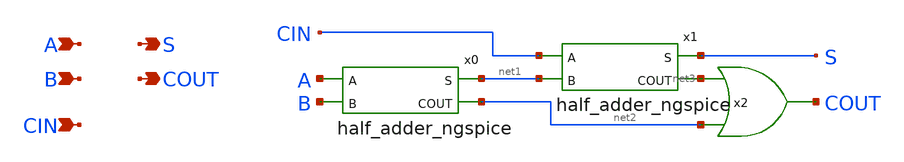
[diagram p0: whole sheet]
** sch_path: xschem_libraries_oa/ngspice/full_adder_ngspice/schematic/full_adder_ngspice.sch
* Copyright (C) 1998-2024 Stefan Frederik Schippers
* This program is free software; you can redistribute it and/or modify
* it under the terms of the GNU General Public License as published by
* the Free Software Foundation; either version 2 of the License, or
* (at your option) any later version.
* This program is distributed in the hope that it will be useful,
* but WITHOUT ANY WARRANTY; without even the implied warranty of
* MERCHANTABILITY or FITNESS FOR A PARTICULAR PURPOSE.  See the
* GNU General Public License for more details.
* You should have received a copy of the GNU General Public License
* along with this program; if not, write to the Free Software
**.subckt full_adder_ngspice A B CIN S COUT
*.ipin A
*.ipin B
*.ipin CIN
*.opin S
*.opin COUT
x0 A net1 net2 B half_adder_ngspice
x1 CIN S net3 net1 half_adder_ngspice
x2 COUT net3 net2 or_ngspice ROUT=1000
**.ends
.end
